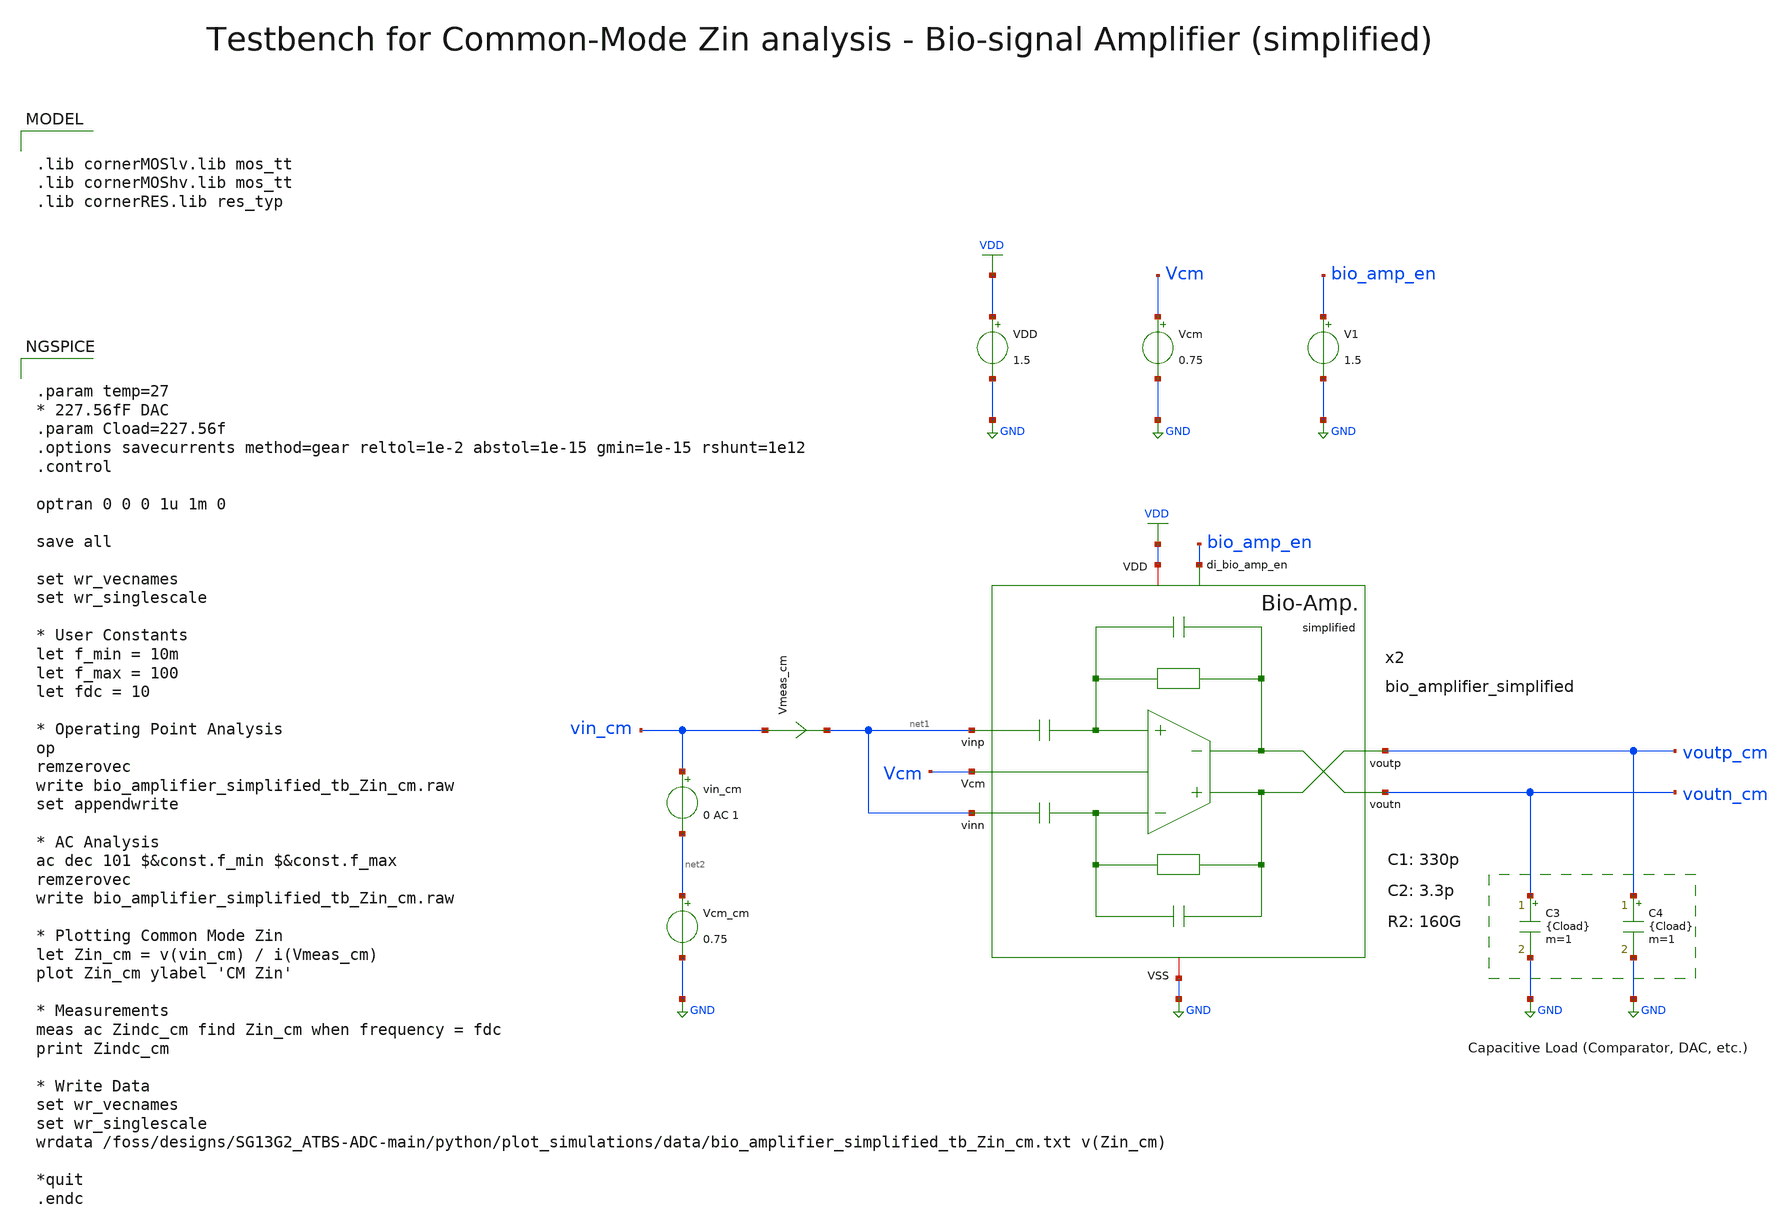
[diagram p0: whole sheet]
** sch_path: SG13G2_ATBS-ADC-main/xschem/bio_amplifier/testbenches/bio_amplifier_simplified_tb_Zin_cm.sch
**.subckt bio_amplifier_simplified_tb_Zin_cm
C3 voutn_cm GND {Cload} m=1
C4 voutp_cm GND {Cload} m=1
vin_cm vin_cm net2 0 AC 1
Vmeas_cm vin_cm net1 0
.save i(vmeas_cm)
Vcm_cm net2 GND 0.75
x2 voutp_cm bio_amp_en net1 Vcm voutn_cm net1 VDD GND bio_amplifier_simplified C1=330p C2=3.3p
+ R2=160G
VDD VDD GND 1.5
Vcm Vcm GND 0.75
V1 bio_amp_en GND 1.5
**** begin user architecture code


.param temp=27
* 227.56fF DAC
.param Cload=227.56f
.options savecurrents method=gear reltol=1e-2 abstol=1e-15 gmin=1e-15 rshunt=1e12
.control

optran 0 0 0 1u 1m 0

save all

set wr_vecnames
set wr_singlescale

* User Constants
let f_min = 10m
let f_max = 100
let fdc = 10

* Operating Point Analysis
op
remzerovec
write bio_amplifier_simplified_tb_Zin_cm.raw
set appendwrite

* AC Analysis
ac dec 101 $&const.f_min $&const.f_max
remzerovec
write bio_amplifier_simplified_tb_Zin_cm.raw

* Plotting Common Mode Zin
let Zin_cm = v(vin_cm) / i(Vmeas_cm)
plot Zin_cm ylabel 'CM Zin'

* Measurements
meas ac Zindc_cm find Zin_cm when frequency = fdc
print Zindc_cm

* Write Data
set wr_vecnames
set wr_singlescale
wrdata
+ /foss/designs/SG13G2_ATBS-ADC-main/python/plot_simulations/data/bio_amplifier_simplified_tb_Zin_cm.txt v(Zin_cm)

*quit
.endc



.lib cornerMOSlv.lib mos_tt
.lib cornerMOShv.lib mos_tt
.lib cornerRES.lib res_typ

**** end user architecture code
**.ends
.GLOBAL GND
.GLOBAL VDD
.end
